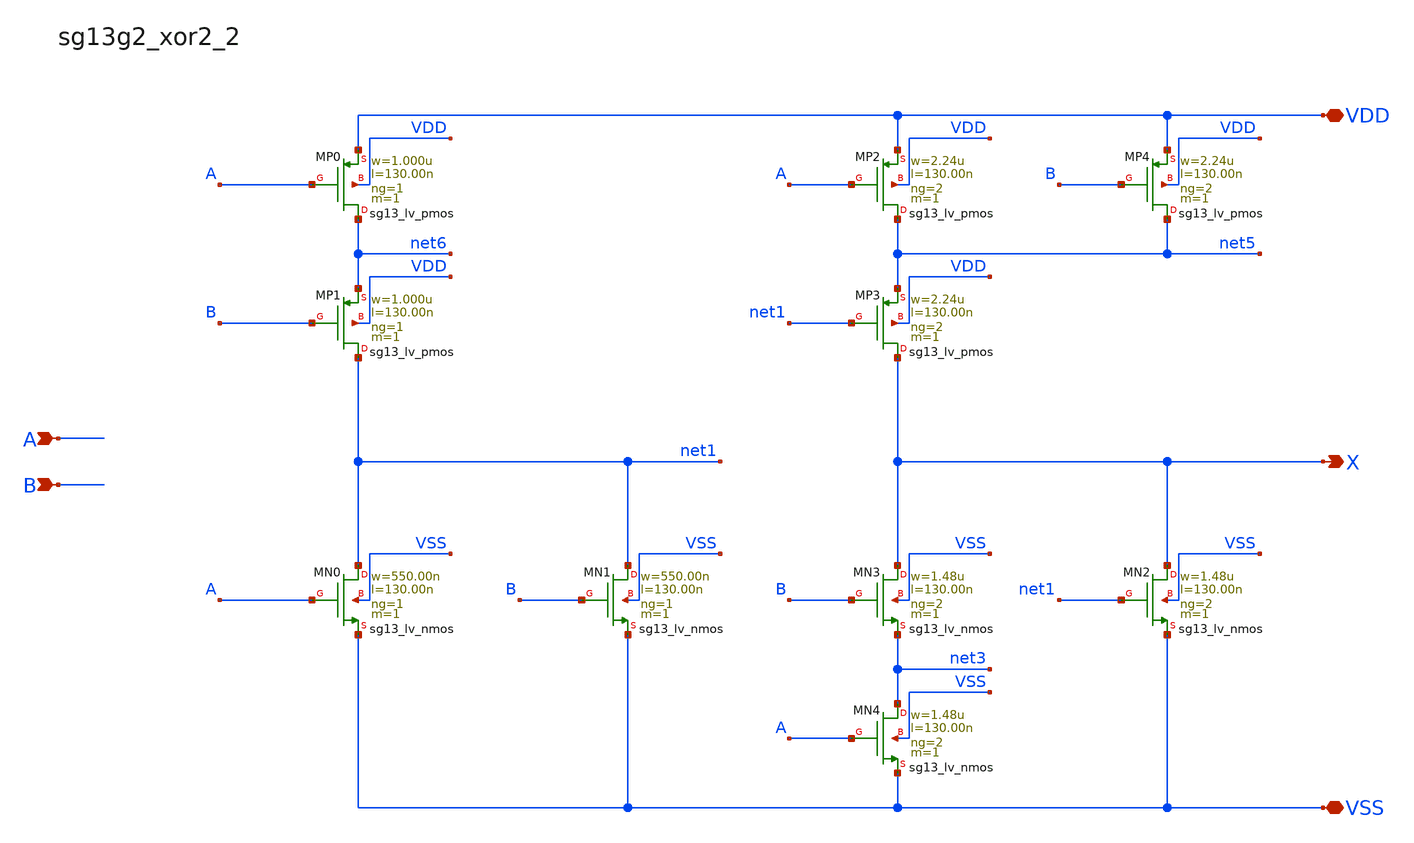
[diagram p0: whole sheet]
** sch_path: outputs/sg13g2_cells/cells/sg13g2_xor2_2/sg13g2_xor2_2.sch
**.subckt sg13g2_xor2_2 X A B VDD VSS
*.opin X
*.ipin A
*.ipin B
*.iopin VDD
*.iopin VSS
XMN0 net1 A VSS VSS sg13_lv_nmos w=550.00n l=130.00n ng=1 m=1 mm_ok=1
XMN3 X B net3 VSS sg13_lv_nmos w=1.48u l=130.00n ng=2 m=1 mm_ok=1
XMN2 X net1 VSS VSS sg13_lv_nmos w=1.48u l=130.00n ng=2 m=1 mm_ok=1
XMN4 net3 A VSS VSS sg13_lv_nmos w=1.48u l=130.00n ng=2 m=1 mm_ok=1
XMN1 net1 B VSS VSS sg13_lv_nmos w=550.00n l=130.00n ng=1 m=1 mm_ok=1
XMP0 net6 A VDD VDD sg13_lv_pmos w=1.000u l=130.00n ng=1 m=1 mm_ok=1
XMP1 net1 B net6 VDD sg13_lv_pmos w=1.000u l=130.00n ng=1 m=1 mm_ok=1
XMP2 net5 A VDD VDD sg13_lv_pmos w=2.24u l=130.00n ng=2 m=1 mm_ok=1
XMP4 net5 B VDD VDD sg13_lv_pmos w=2.24u l=130.00n ng=2 m=1 mm_ok=1
XMP3 X net1 net5 VDD sg13_lv_pmos w=2.24u l=130.00n ng=2 m=1 mm_ok=1
**.ends
.end
